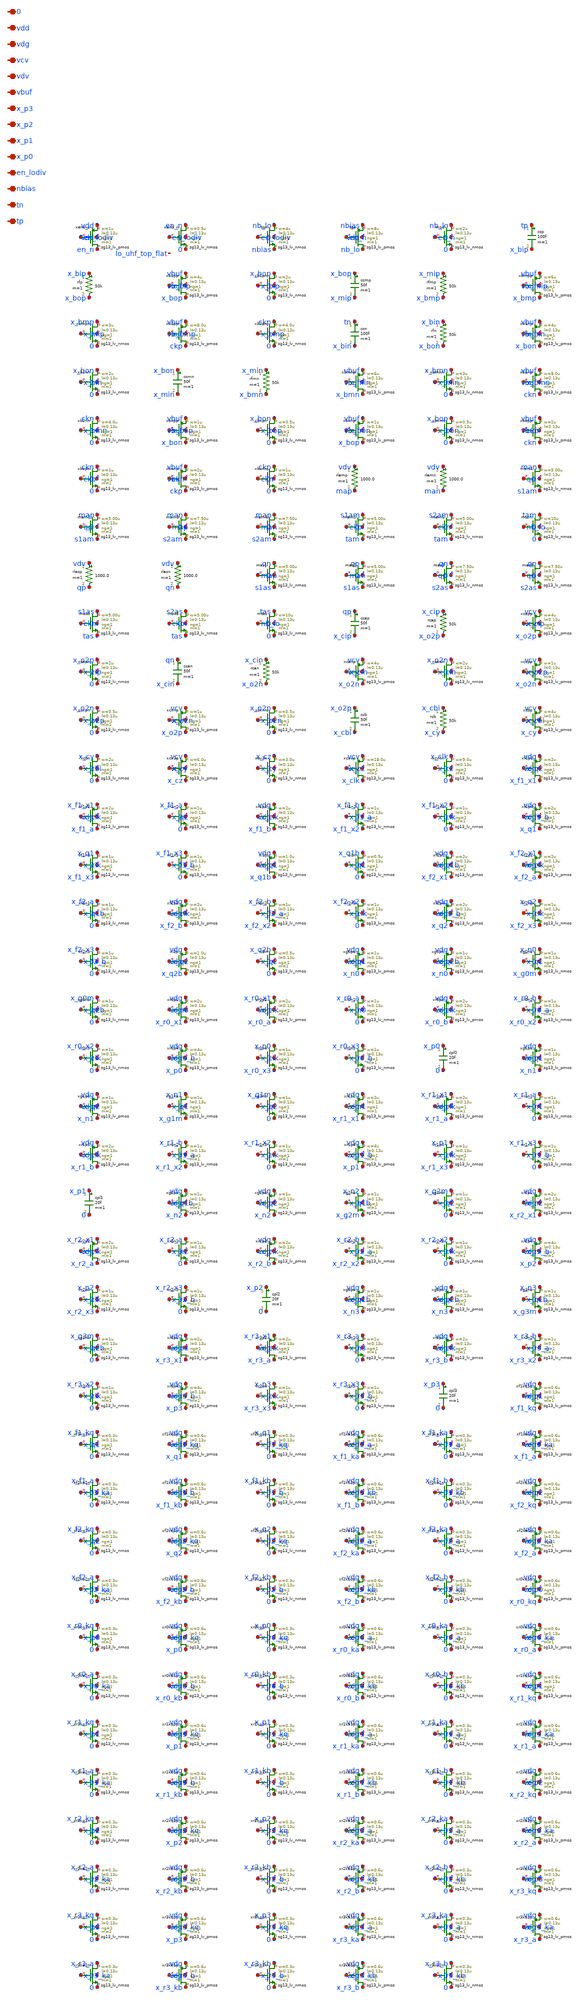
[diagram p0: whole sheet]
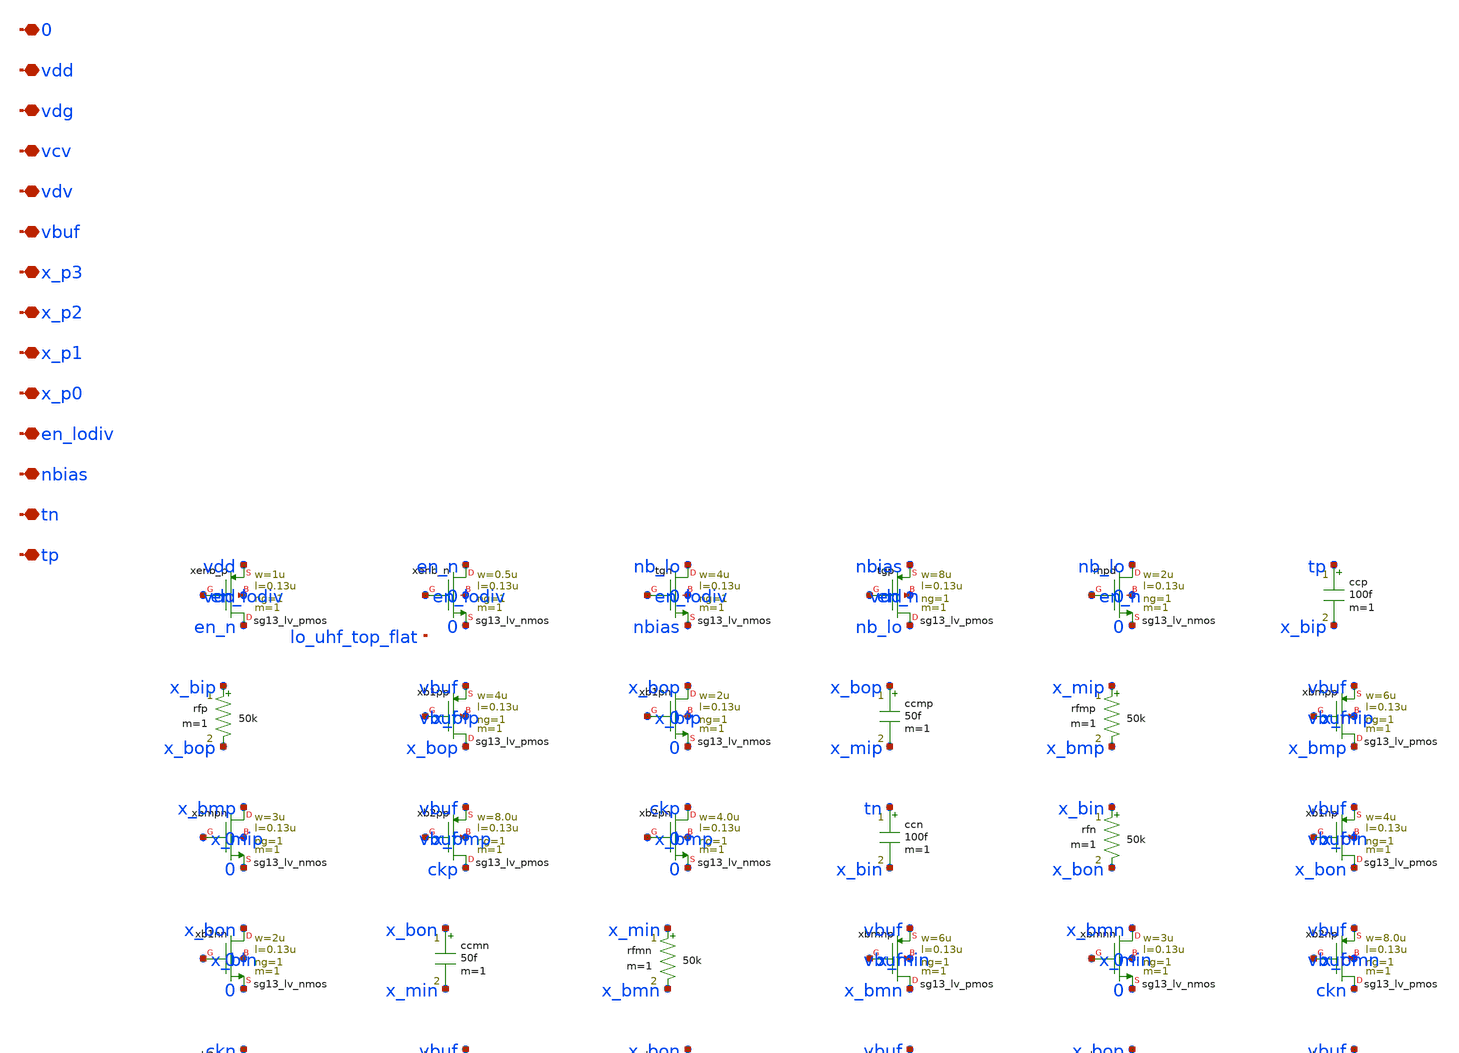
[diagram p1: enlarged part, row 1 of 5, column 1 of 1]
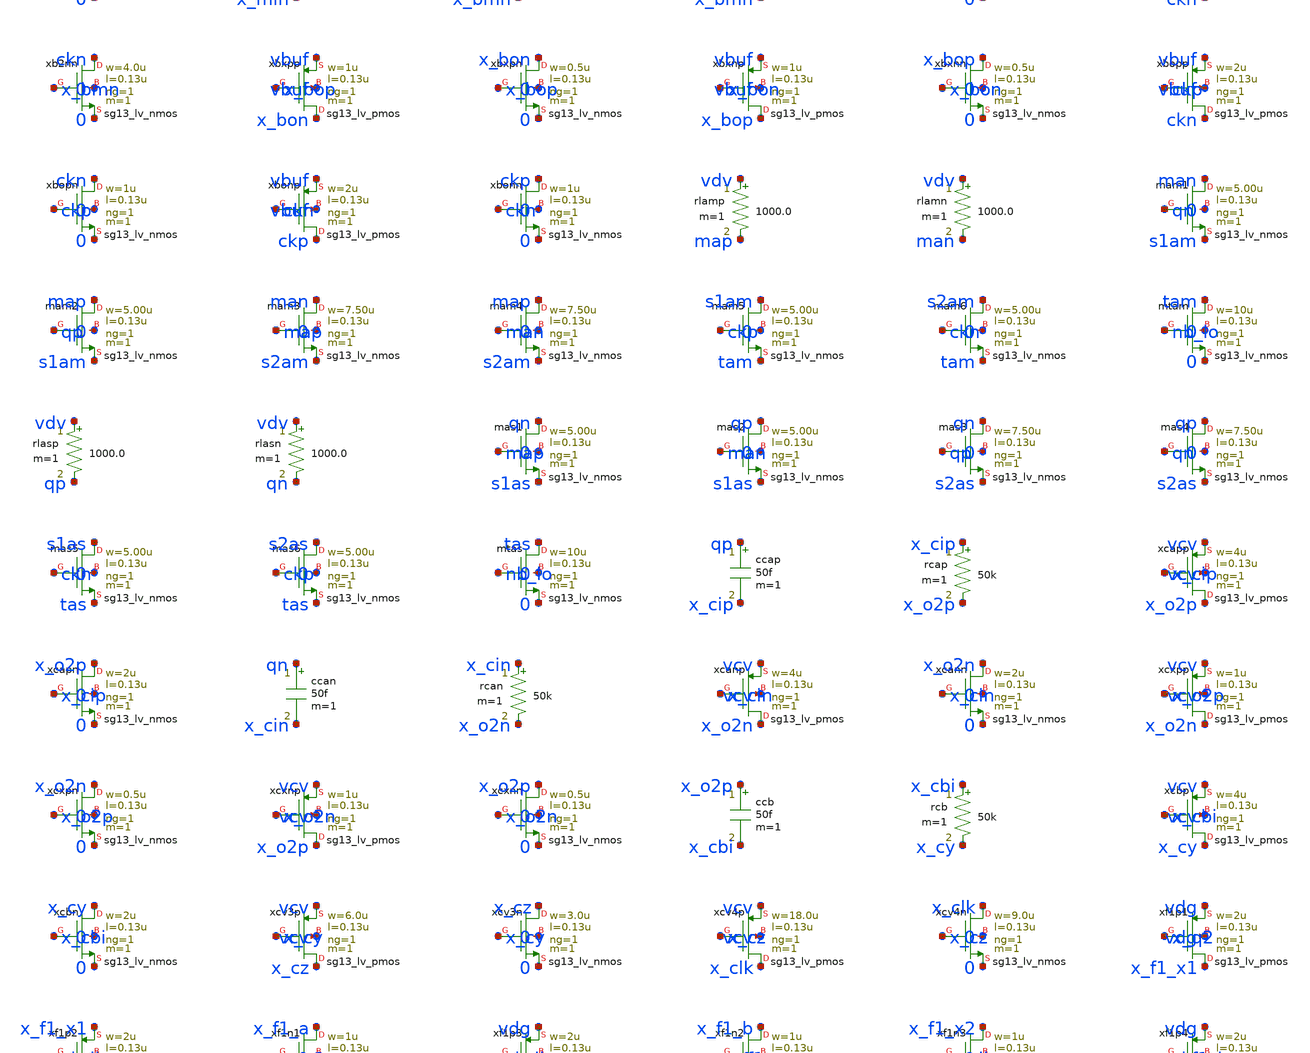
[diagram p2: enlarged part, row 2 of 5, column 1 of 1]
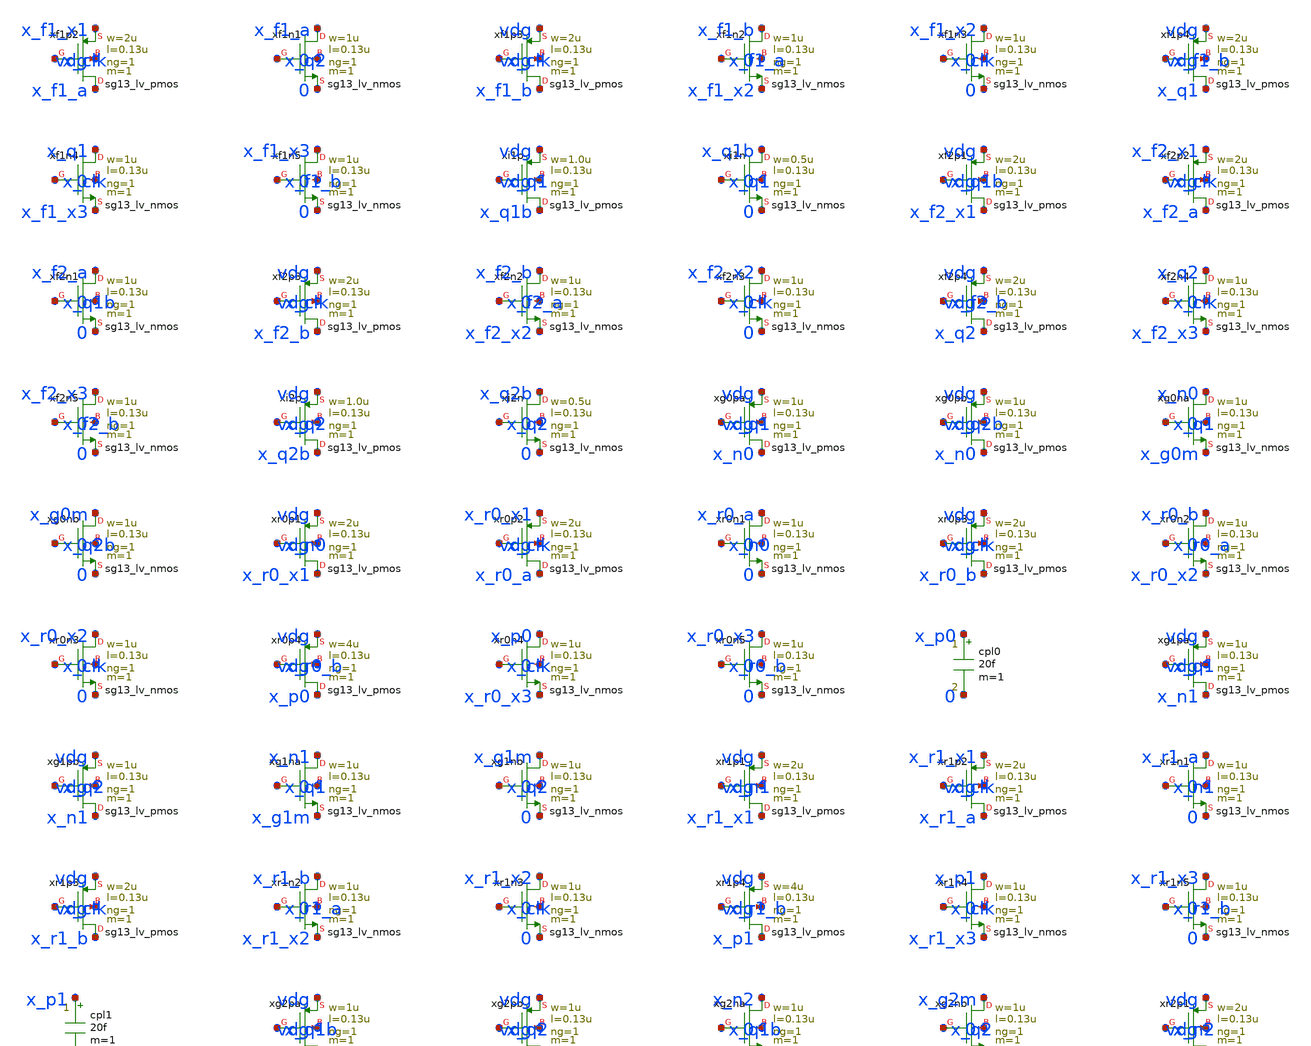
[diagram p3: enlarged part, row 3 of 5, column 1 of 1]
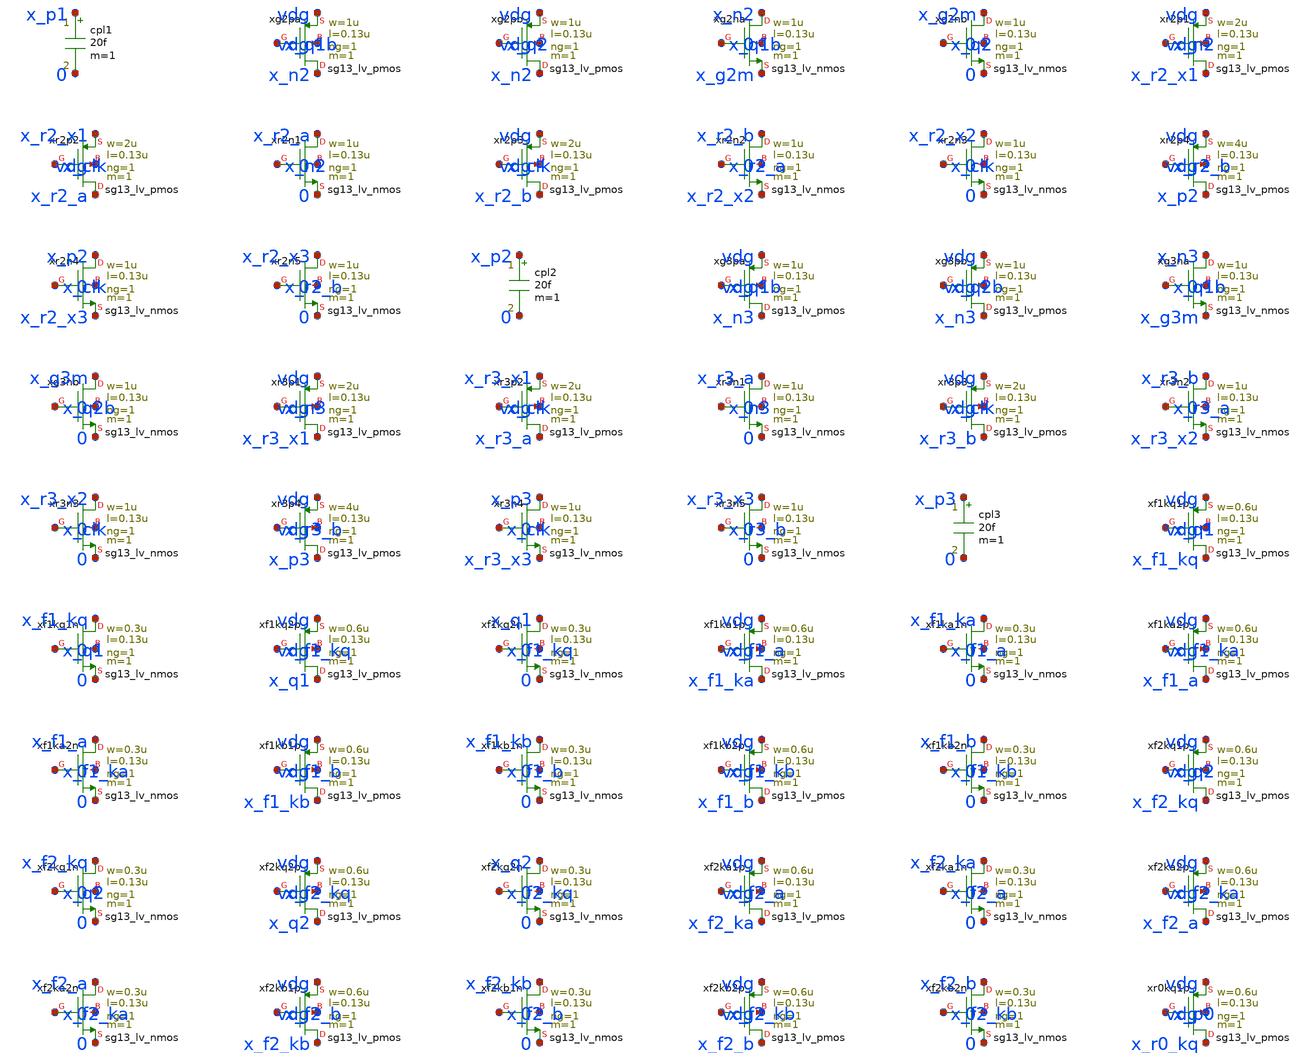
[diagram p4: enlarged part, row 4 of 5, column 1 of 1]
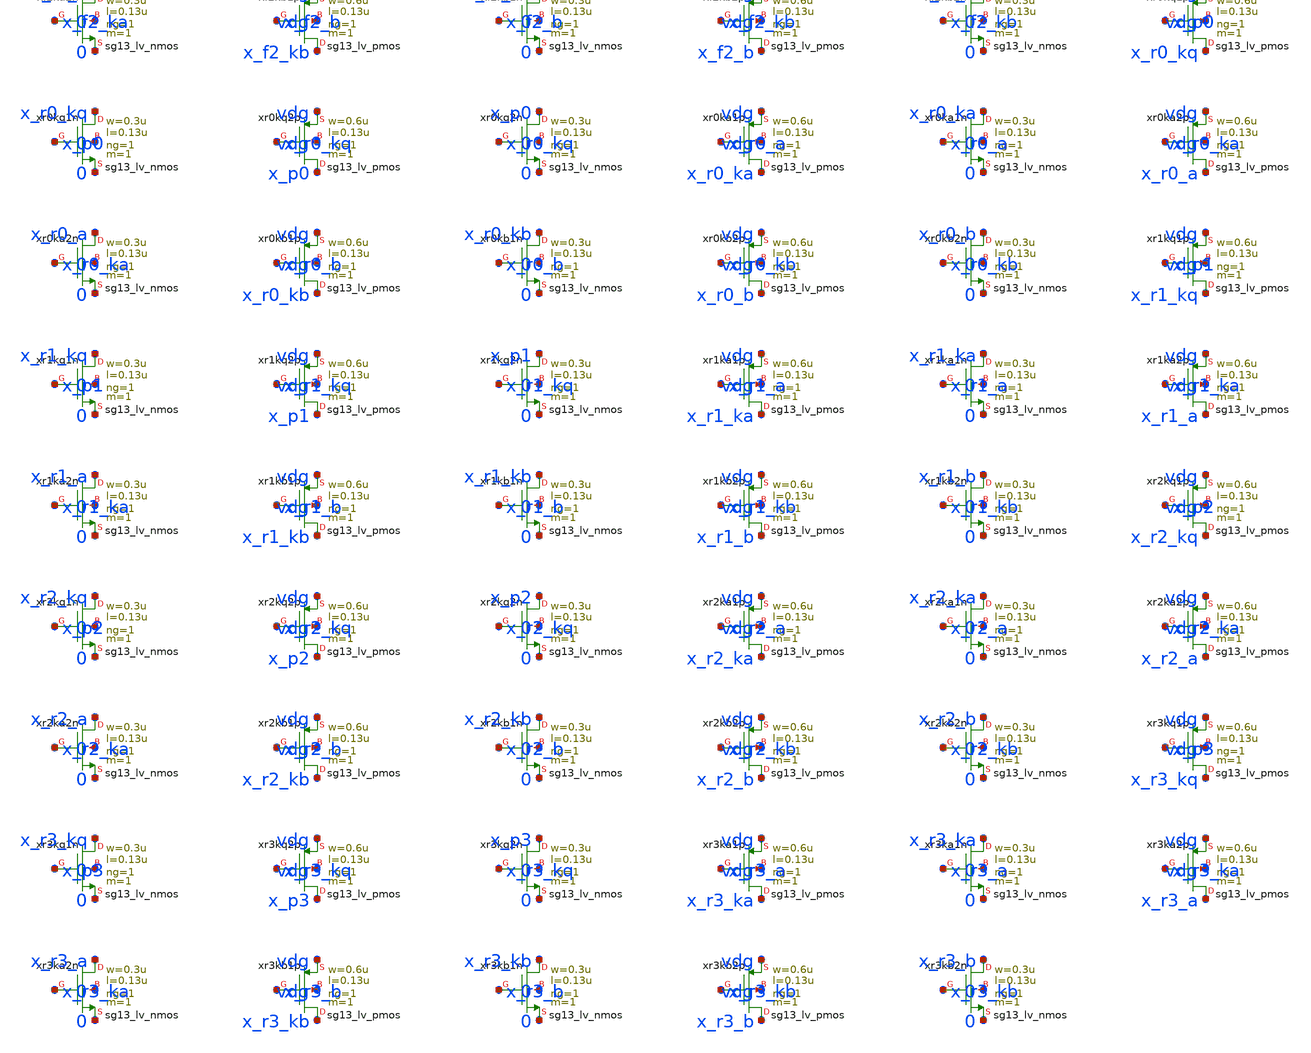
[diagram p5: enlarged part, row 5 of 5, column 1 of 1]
** sch_path: analog/lo/sch/lo_uhf_top.sch
**.subckt lo_uhf_top tp tn nbias en_lodiv x_p0 x_p1 x_p2 x_p3 vbuf vdv vcv vdg vdd 0
*.iopin tp
*.iopin tn
*.iopin nbias
*.iopin en_lodiv
*.iopin x_p0
*.iopin x_p1
*.iopin x_p2
*.iopin x_p3
*.iopin vbuf
*.iopin vdv
*.iopin vcv
*.iopin vdg
*.iopin vdd
*.iopin 0
Xxenb_p en_n en_lodiv vdd vdd sg13_lv_pmos w=1u l=0.13u ng=1 m=1 mm_ok=1
Xxenb_n en_n en_lodiv 0 0 sg13_lv_nmos w=0.5u l=0.13u ng=1 m=1 mm_ok=1
Xtgn nb_lo en_lodiv nbias 0 sg13_lv_nmos w=4u l=0.13u ng=1 m=1 mm_ok=1
Xtgp nb_lo en_n nbias vdd sg13_lv_pmos w=8u l=0.13u ng=1 m=1 mm_ok=1
Xmpd nb_lo en_n 0 0 sg13_lv_nmos w=2u l=0.13u ng=1 m=1 mm_ok=1
ccp tp x_bip 100f m=1
rfp x_bip x_bop 50k m=1
Xxb1pp x_bop x_bip vbuf vbuf sg13_lv_pmos w=4u l=0.13u ng=1 m=1 mm_ok=1
Xxb1pn x_bop x_bip 0 0 sg13_lv_nmos w=2u l=0.13u ng=1 m=1 mm_ok=1
ccmp x_bop x_mip 50f m=1
rfmp x_mip x_bmp 50k m=1
Xxbmpp x_bmp x_mip vbuf vbuf sg13_lv_pmos w=6u l=0.13u ng=1 m=1 mm_ok=1
Xxbmpn x_bmp x_mip 0 0 sg13_lv_nmos w=3u l=0.13u ng=1 m=1 mm_ok=1
Xxb2pp ckp x_bmp vbuf vbuf sg13_lv_pmos w=8.0u l=0.13u ng=1 m=1 mm_ok=1
Xxb2pn ckp x_bmp 0 0 sg13_lv_nmos w=4.0u l=0.13u ng=1 m=1 mm_ok=1
ccn tn x_bin 100f m=1
rfn x_bin x_bon 50k m=1
Xxb1np x_bon x_bin vbuf vbuf sg13_lv_pmos w=4u l=0.13u ng=1 m=1 mm_ok=1
Xxb1nn x_bon x_bin 0 0 sg13_lv_nmos w=2u l=0.13u ng=1 m=1 mm_ok=1
ccmn x_bon x_min 50f m=1
rfmn x_min x_bmn 50k m=1
Xxbmnp x_bmn x_min vbuf vbuf sg13_lv_pmos w=6u l=0.13u ng=1 m=1 mm_ok=1
Xxbmnn x_bmn x_min 0 0 sg13_lv_nmos w=3u l=0.13u ng=1 m=1 mm_ok=1
Xxb2np ckn x_bmn vbuf vbuf sg13_lv_pmos w=8.0u l=0.13u ng=1 m=1 mm_ok=1
Xxb2nn ckn x_bmn 0 0 sg13_lv_nmos w=4.0u l=0.13u ng=1 m=1 mm_ok=1
Xxbxpp x_bon x_bop vbuf vbuf sg13_lv_pmos w=1u l=0.13u ng=1 m=1 mm_ok=1
Xxbxpn x_bon x_bop 0 0 sg13_lv_nmos w=0.5u l=0.13u ng=1 m=1 mm_ok=1
Xxbxnp x_bop x_bon vbuf vbuf sg13_lv_pmos w=1u l=0.13u ng=1 m=1 mm_ok=1
Xxbxnn x_bop x_bon 0 0 sg13_lv_nmos w=0.5u l=0.13u ng=1 m=1 mm_ok=1
Xxbopp ckn ckp vbuf vbuf sg13_lv_pmos w=2u l=0.13u ng=1 m=1 mm_ok=1
Xxbopn ckn ckp 0 0 sg13_lv_nmos w=1u l=0.13u ng=1 m=1 mm_ok=1
Xxbonp ckp ckn vbuf vbuf sg13_lv_pmos w=2u l=0.13u ng=1 m=1 mm_ok=1
Xxbonn ckp ckn 0 0 sg13_lv_nmos w=1u l=0.13u ng=1 m=1 mm_ok=1
rlamp vdv map 1000.0 m=1
rlamn vdv man 1000.0 m=1
Xmam1 man qn s1am 0 sg13_lv_nmos w=5.00u l=0.13u ng=1 m=1 mm_ok=1
Xmam2 map qp s1am 0 sg13_lv_nmos w=5.00u l=0.13u ng=1 m=1 mm_ok=1
Xmam3 man map s2am 0 sg13_lv_nmos w=7.50u l=0.13u ng=1 m=1 mm_ok=1
Xmam4 map man s2am 0 sg13_lv_nmos w=7.50u l=0.13u ng=1 m=1 mm_ok=1
Xmam5 s1am ckp tam 0 sg13_lv_nmos w=5.00u l=0.13u ng=1 m=1 mm_ok=1
Xmam6 s2am ckn tam 0 sg13_lv_nmos w=5.00u l=0.13u ng=1 m=1 mm_ok=1
Xmtam tam nb_lo 0 0 sg13_lv_nmos w=10u l=0.13u ng=1 m=1 mm_ok=1
rlasp vdv qp 1000.0 m=1
rlasn vdv qn 1000.0 m=1
Xmas1 qn map s1as 0 sg13_lv_nmos w=5.00u l=0.13u ng=1 m=1 mm_ok=1
Xmas2 qp man s1as 0 sg13_lv_nmos w=5.00u l=0.13u ng=1 m=1 mm_ok=1
Xmas3 qn qp s2as 0 sg13_lv_nmos w=7.50u l=0.13u ng=1 m=1 mm_ok=1
Xmas4 qp qn s2as 0 sg13_lv_nmos w=7.50u l=0.13u ng=1 m=1 mm_ok=1
Xmas5 s1as ckn tas 0 sg13_lv_nmos w=5.00u l=0.13u ng=1 m=1 mm_ok=1
Xmas6 s2as ckp tas 0 sg13_lv_nmos w=5.00u l=0.13u ng=1 m=1 mm_ok=1
Xmtas tas nb_lo 0 0 sg13_lv_nmos w=10u l=0.13u ng=1 m=1 mm_ok=1
ccap qp x_cip 50f m=1
rcap x_cip x_o2p 50k m=1
Xxcapp x_o2p x_cip vcv vcv sg13_lv_pmos w=4u l=0.13u ng=1 m=1 mm_ok=1
Xxcapn x_o2p x_cip 0 0 sg13_lv_nmos w=2u l=0.13u ng=1 m=1 mm_ok=1
ccan qn x_cin 50f m=1
rcan x_cin x_o2n 50k m=1
Xxcanp x_o2n x_cin vcv vcv sg13_lv_pmos w=4u l=0.13u ng=1 m=1 mm_ok=1
Xxcann x_o2n x_cin 0 0 sg13_lv_nmos w=2u l=0.13u ng=1 m=1 mm_ok=1
Xxcxpp x_o2n x_o2p vcv vcv sg13_lv_pmos w=1u l=0.13u ng=1 m=1 mm_ok=1
Xxcxpn x_o2n x_o2p 0 0 sg13_lv_nmos w=0.5u l=0.13u ng=1 m=1 mm_ok=1
Xxcxnp x_o2p x_o2n vcv vcv sg13_lv_pmos w=1u l=0.13u ng=1 m=1 mm_ok=1
Xxcxnn x_o2p x_o2n 0 0 sg13_lv_nmos w=0.5u l=0.13u ng=1 m=1 mm_ok=1
ccb x_o2p x_cbi 50f m=1
rcb x_cbi x_cy 50k m=1
Xxcbp x_cy x_cbi vcv vcv sg13_lv_pmos w=4u l=0.13u ng=1 m=1 mm_ok=1
Xxcbn x_cy x_cbi 0 0 sg13_lv_nmos w=2u l=0.13u ng=1 m=1 mm_ok=1
Xxcv3p x_cz x_cy vcv vcv sg13_lv_pmos w=6.0u l=0.13u ng=1 m=1 mm_ok=1
Xxcv3n x_cz x_cy 0 0 sg13_lv_nmos w=3.0u l=0.13u ng=1 m=1 mm_ok=1
Xxcv4p x_clk x_cz vcv vcv sg13_lv_pmos w=18.0u l=0.13u ng=1 m=1 mm_ok=1
Xxcv4n x_clk x_cz 0 0 sg13_lv_nmos w=9.0u l=0.13u ng=1 m=1 mm_ok=1
Xxf1p1 x_f1_x1 x_q2 vdg vdg sg13_lv_pmos w=2u l=0.13u ng=1 m=1 mm_ok=1
Xxf1p2 x_f1_a x_clk x_f1_x1 vdg sg13_lv_pmos w=2u l=0.13u ng=1 m=1 mm_ok=1
Xxf1n1 x_f1_a x_q2 0 0 sg13_lv_nmos w=1u l=0.13u ng=1 m=1 mm_ok=1
Xxf1p3 x_f1_b x_clk vdg vdg sg13_lv_pmos w=2u l=0.13u ng=1 m=1 mm_ok=1
Xxf1n2 x_f1_b x_f1_a x_f1_x2 0 sg13_lv_nmos w=1u l=0.13u ng=1 m=1 mm_ok=1
Xxf1n3 x_f1_x2 x_clk 0 0 sg13_lv_nmos w=1u l=0.13u ng=1 m=1 mm_ok=1
Xxf1p4 x_q1 x_f1_b vdg vdg sg13_lv_pmos w=2u l=0.13u ng=1 m=1 mm_ok=1
Xxf1n4 x_q1 x_clk x_f1_x3 0 sg13_lv_nmos w=1u l=0.13u ng=1 m=1 mm_ok=1
Xxf1n5 x_f1_x3 x_f1_b 0 0 sg13_lv_nmos w=1u l=0.13u ng=1 m=1 mm_ok=1
Xxi1p x_q1b x_q1 vdg vdg sg13_lv_pmos w=1.0u l=0.13u ng=1 m=1 mm_ok=1
Xxi1n x_q1b x_q1 0 0 sg13_lv_nmos w=0.5u l=0.13u ng=1 m=1 mm_ok=1
Xxf2p1 x_f2_x1 x_q1b vdg vdg sg13_lv_pmos w=2u l=0.13u ng=1 m=1 mm_ok=1
Xxf2p2 x_f2_a x_clk x_f2_x1 vdg sg13_lv_pmos w=2u l=0.13u ng=1 m=1 mm_ok=1
Xxf2n1 x_f2_a x_q1b 0 0 sg13_lv_nmos w=1u l=0.13u ng=1 m=1 mm_ok=1
Xxf2p3 x_f2_b x_clk vdg vdg sg13_lv_pmos w=2u l=0.13u ng=1 m=1 mm_ok=1
Xxf2n2 x_f2_b x_f2_a x_f2_x2 0 sg13_lv_nmos w=1u l=0.13u ng=1 m=1 mm_ok=1
Xxf2n3 x_f2_x2 x_clk 0 0 sg13_lv_nmos w=1u l=0.13u ng=1 m=1 mm_ok=1
Xxf2p4 x_q2 x_f2_b vdg vdg sg13_lv_pmos w=2u l=0.13u ng=1 m=1 mm_ok=1
Xxf2n4 x_q2 x_clk x_f2_x3 0 sg13_lv_nmos w=1u l=0.13u ng=1 m=1 mm_ok=1
Xxf2n5 x_f2_x3 x_f2_b 0 0 sg13_lv_nmos w=1u l=0.13u ng=1 m=1 mm_ok=1
Xxi2p x_q2b x_q2 vdg vdg sg13_lv_pmos w=1.0u l=0.13u ng=1 m=1 mm_ok=1
Xxi2n x_q2b x_q2 0 0 sg13_lv_nmos w=0.5u l=0.13u ng=1 m=1 mm_ok=1
Xxg0pa x_n0 x_q1 vdg vdg sg13_lv_pmos w=1u l=0.13u ng=1 m=1 mm_ok=1
Xxg0pb x_n0 x_q2b vdg vdg sg13_lv_pmos w=1u l=0.13u ng=1 m=1 mm_ok=1
Xxg0na x_n0 x_q1 x_g0m 0 sg13_lv_nmos w=1u l=0.13u ng=1 m=1 mm_ok=1
Xxg0nb x_g0m x_q2b 0 0 sg13_lv_nmos w=1u l=0.13u ng=1 m=1 mm_ok=1
Xxr0p1 x_r0_x1 x_n0 vdg vdg sg13_lv_pmos w=2u l=0.13u ng=1 m=1 mm_ok=1
Xxr0p2 x_r0_a x_clk x_r0_x1 vdg sg13_lv_pmos w=2u l=0.13u ng=1 m=1 mm_ok=1
Xxr0n1 x_r0_a x_n0 0 0 sg13_lv_nmos w=1u l=0.13u ng=1 m=1 mm_ok=1
Xxr0p3 x_r0_b x_clk vdg vdg sg13_lv_pmos w=2u l=0.13u ng=1 m=1 mm_ok=1
Xxr0n2 x_r0_b x_r0_a x_r0_x2 0 sg13_lv_nmos w=1u l=0.13u ng=1 m=1 mm_ok=1
Xxr0n3 x_r0_x2 x_clk 0 0 sg13_lv_nmos w=1u l=0.13u ng=1 m=1 mm_ok=1
Xxr0p4 x_p0 x_r0_b vdg vdg sg13_lv_pmos w=4u l=0.13u ng=1 m=1 mm_ok=1
Xxr0n4 x_p0 x_clk x_r0_x3 0 sg13_lv_nmos w=1u l=0.13u ng=1 m=1 mm_ok=1
Xxr0n5 x_r0_x3 x_r0_b 0 0 sg13_lv_nmos w=1u l=0.13u ng=1 m=1 mm_ok=1
cpl0 x_p0 0 20f m=1
Xxg1pa x_n1 x_q1 vdg vdg sg13_lv_pmos w=1u l=0.13u ng=1 m=1 mm_ok=1
Xxg1pb x_n1 x_q2 vdg vdg sg13_lv_pmos w=1u l=0.13u ng=1 m=1 mm_ok=1
Xxg1na x_n1 x_q1 x_g1m 0 sg13_lv_nmos w=1u l=0.13u ng=1 m=1 mm_ok=1
Xxg1nb x_g1m x_q2 0 0 sg13_lv_nmos w=1u l=0.13u ng=1 m=1 mm_ok=1
Xxr1p1 x_r1_x1 x_n1 vdg vdg sg13_lv_pmos w=2u l=0.13u ng=1 m=1 mm_ok=1
Xxr1p2 x_r1_a x_clk x_r1_x1 vdg sg13_lv_pmos w=2u l=0.13u ng=1 m=1 mm_ok=1
Xxr1n1 x_r1_a x_n1 0 0 sg13_lv_nmos w=1u l=0.13u ng=1 m=1 mm_ok=1
Xxr1p3 x_r1_b x_clk vdg vdg sg13_lv_pmos w=2u l=0.13u ng=1 m=1 mm_ok=1
Xxr1n2 x_r1_b x_r1_a x_r1_x2 0 sg13_lv_nmos w=1u l=0.13u ng=1 m=1 mm_ok=1
Xxr1n3 x_r1_x2 x_clk 0 0 sg13_lv_nmos w=1u l=0.13u ng=1 m=1 mm_ok=1
Xxr1p4 x_p1 x_r1_b vdg vdg sg13_lv_pmos w=4u l=0.13u ng=1 m=1 mm_ok=1
Xxr1n4 x_p1 x_clk x_r1_x3 0 sg13_lv_nmos w=1u l=0.13u ng=1 m=1 mm_ok=1
Xxr1n5 x_r1_x3 x_r1_b 0 0 sg13_lv_nmos w=1u l=0.13u ng=1 m=1 mm_ok=1
cpl1 x_p1 0 20f m=1
Xxg2pa x_n2 x_q1b vdg vdg sg13_lv_pmos w=1u l=0.13u ng=1 m=1 mm_ok=1
Xxg2pb x_n2 x_q2 vdg vdg sg13_lv_pmos w=1u l=0.13u ng=1 m=1 mm_ok=1
Xxg2na x_n2 x_q1b x_g2m 0 sg13_lv_nmos w=1u l=0.13u ng=1 m=1 mm_ok=1
Xxg2nb x_g2m x_q2 0 0 sg13_lv_nmos w=1u l=0.13u ng=1 m=1 mm_ok=1
Xxr2p1 x_r2_x1 x_n2 vdg vdg sg13_lv_pmos w=2u l=0.13u ng=1 m=1 mm_ok=1
Xxr2p2 x_r2_a x_clk x_r2_x1 vdg sg13_lv_pmos w=2u l=0.13u ng=1 m=1 mm_ok=1
Xxr2n1 x_r2_a x_n2 0 0 sg13_lv_nmos w=1u l=0.13u ng=1 m=1 mm_ok=1
Xxr2p3 x_r2_b x_clk vdg vdg sg13_lv_pmos w=2u l=0.13u ng=1 m=1 mm_ok=1
Xxr2n2 x_r2_b x_r2_a x_r2_x2 0 sg13_lv_nmos w=1u l=0.13u ng=1 m=1 mm_ok=1
Xxr2n3 x_r2_x2 x_clk 0 0 sg13_lv_nmos w=1u l=0.13u ng=1 m=1 mm_ok=1
Xxr2p4 x_p2 x_r2_b vdg vdg sg13_lv_pmos w=4u l=0.13u ng=1 m=1 mm_ok=1
Xxr2n4 x_p2 x_clk x_r2_x3 0 sg13_lv_nmos w=1u l=0.13u ng=1 m=1 mm_ok=1
Xxr2n5 x_r2_x3 x_r2_b 0 0 sg13_lv_nmos w=1u l=0.13u ng=1 m=1 mm_ok=1
cpl2 x_p2 0 20f m=1
Xxg3pa x_n3 x_q1b vdg vdg sg13_lv_pmos w=1u l=0.13u ng=1 m=1 mm_ok=1
Xxg3pb x_n3 x_q2b vdg vdg sg13_lv_pmos w=1u l=0.13u ng=1 m=1 mm_ok=1
Xxg3na x_n3 x_q1b x_g3m 0 sg13_lv_nmos w=1u l=0.13u ng=1 m=1 mm_ok=1
Xxg3nb x_g3m x_q2b 0 0 sg13_lv_nmos w=1u l=0.13u ng=1 m=1 mm_ok=1
Xxr3p1 x_r3_x1 x_n3 vdg vdg sg13_lv_pmos w=2u l=0.13u ng=1 m=1 mm_ok=1
Xxr3p2 x_r3_a x_clk x_r3_x1 vdg sg13_lv_pmos w=2u l=0.13u ng=1 m=1 mm_ok=1
Xxr3n1 x_r3_a x_n3 0 0 sg13_lv_nmos w=1u l=0.13u ng=1 m=1 mm_ok=1
Xxr3p3 x_r3_b x_clk vdg vdg sg13_lv_pmos w=2u l=0.13u ng=1 m=1 mm_ok=1
Xxr3n2 x_r3_b x_r3_a x_r3_x2 0 sg13_lv_nmos w=1u l=0.13u ng=1 m=1 mm_ok=1
Xxr3n3 x_r3_x2 x_clk 0 0 sg13_lv_nmos w=1u l=0.13u ng=1 m=1 mm_ok=1
Xxr3p4 x_p3 x_r3_b vdg vdg sg13_lv_pmos w=4u l=0.13u ng=1 m=1 mm_ok=1
Xxr3n4 x_p3 x_clk x_r3_x3 0 sg13_lv_nmos w=1u l=0.13u ng=1 m=1 mm_ok=1
Xxr3n5 x_r3_x3 x_r3_b 0 0 sg13_lv_nmos w=1u l=0.13u ng=1 m=1 mm_ok=1
cpl3 x_p3 0 20f m=1
Xxf1kq1p x_f1_kq x_q1 vdg vdg sg13_lv_pmos w=0.6u l=0.13u ng=1 m=1 mm_ok=1
Xxf1kq1n x_f1_kq x_q1 0 0 sg13_lv_nmos w=0.3u l=0.13u ng=1 m=1 mm_ok=1
Xxf1kq2p x_q1 x_f1_kq vdg vdg sg13_lv_pmos w=0.6u l=0.13u ng=1 m=1 mm_ok=1
Xxf1kq2n x_q1 x_f1_kq 0 0 sg13_lv_nmos w=0.3u l=0.13u ng=1 m=1 mm_ok=1
Xxf1ka1p x_f1_ka x_f1_a vdg vdg sg13_lv_pmos w=0.6u l=0.13u ng=1 m=1 mm_ok=1
Xxf1ka1n x_f1_ka x_f1_a 0 0 sg13_lv_nmos w=0.3u l=0.13u ng=1 m=1 mm_ok=1
Xxf1ka2p x_f1_a x_f1_ka vdg vdg sg13_lv_pmos w=0.6u l=0.13u ng=1 m=1 mm_ok=1
Xxf1ka2n x_f1_a x_f1_ka 0 0 sg13_lv_nmos w=0.3u l=0.13u ng=1 m=1 mm_ok=1
Xxf1kb1p x_f1_kb x_f1_b vdg vdg sg13_lv_pmos w=0.6u l=0.13u ng=1 m=1 mm_ok=1
Xxf1kb1n x_f1_kb x_f1_b 0 0 sg13_lv_nmos w=0.3u l=0.13u ng=1 m=1 mm_ok=1
Xxf1kb2p x_f1_b x_f1_kb vdg vdg sg13_lv_pmos w=0.6u l=0.13u ng=1 m=1 mm_ok=1
Xxf1kb2n x_f1_b x_f1_kb 0 0 sg13_lv_nmos w=0.3u l=0.13u ng=1 m=1 mm_ok=1
Xxf2kq1p x_f2_kq x_q2 vdg vdg sg13_lv_pmos w=0.6u l=0.13u ng=1 m=1 mm_ok=1
Xxf2kq1n x_f2_kq x_q2 0 0 sg13_lv_nmos w=0.3u l=0.13u ng=1 m=1 mm_ok=1
Xxf2kq2p x_q2 x_f2_kq vdg vdg sg13_lv_pmos w=0.6u l=0.13u ng=1 m=1 mm_ok=1
Xxf2kq2n x_q2 x_f2_kq 0 0 sg13_lv_nmos w=0.3u l=0.13u ng=1 m=1 mm_ok=1
Xxf2ka1p x_f2_ka x_f2_a vdg vdg sg13_lv_pmos w=0.6u l=0.13u ng=1 m=1 mm_ok=1
Xxf2ka1n x_f2_ka x_f2_a 0 0 sg13_lv_nmos w=0.3u l=0.13u ng=1 m=1 mm_ok=1
Xxf2ka2p x_f2_a x_f2_ka vdg vdg sg13_lv_pmos w=0.6u l=0.13u ng=1 m=1 mm_ok=1
Xxf2ka2n x_f2_a x_f2_ka 0 0 sg13_lv_nmos w=0.3u l=0.13u ng=1 m=1 mm_ok=1
Xxf2kb1p x_f2_kb x_f2_b vdg vdg sg13_lv_pmos w=0.6u l=0.13u ng=1 m=1 mm_ok=1
Xxf2kb1n x_f2_kb x_f2_b 0 0 sg13_lv_nmos w=0.3u l=0.13u ng=1 m=1 mm_ok=1
Xxf2kb2p x_f2_b x_f2_kb vdg vdg sg13_lv_pmos w=0.6u l=0.13u ng=1 m=1 mm_ok=1
Xxf2kb2n x_f2_b x_f2_kb 0 0 sg13_lv_nmos w=0.3u l=0.13u ng=1 m=1 mm_ok=1
Xxr0kq1p x_r0_kq x_p0 vdg vdg sg13_lv_pmos w=0.6u l=0.13u ng=1 m=1 mm_ok=1
Xxr0kq1n x_r0_kq x_p0 0 0 sg13_lv_nmos w=0.3u l=0.13u ng=1 m=1 mm_ok=1
Xxr0kq2p x_p0 x_r0_kq vdg vdg sg13_lv_pmos w=0.6u l=0.13u ng=1 m=1 mm_ok=1
Xxr0kq2n x_p0 x_r0_kq 0 0 sg13_lv_nmos w=0.3u l=0.13u ng=1 m=1 mm_ok=1
Xxr0ka1p x_r0_ka x_r0_a vdg vdg sg13_lv_pmos w=0.6u l=0.13u ng=1 m=1 mm_ok=1
Xxr0ka1n x_r0_ka x_r0_a 0 0 sg13_lv_nmos w=0.3u l=0.13u ng=1 m=1 mm_ok=1
Xxr0ka2p x_r0_a x_r0_ka vdg vdg sg13_lv_pmos w=0.6u l=0.13u ng=1 m=1 mm_ok=1
Xxr0ka2n x_r0_a x_r0_ka 0 0 sg13_lv_nmos w=0.3u l=0.13u ng=1 m=1 mm_ok=1
Xxr0kb1p x_r0_kb x_r0_b vdg vdg sg13_lv_pmos w=0.6u l=0.13u ng=1 m=1 mm_ok=1
Xxr0kb1n x_r0_kb x_r0_b 0 0 sg13_lv_nmos w=0.3u l=0.13u ng=1 m=1 mm_ok=1
Xxr0kb2p x_r0_b x_r0_kb vdg vdg sg13_lv_pmos w=0.6u l=0.13u ng=1 m=1 mm_ok=1
Xxr0kb2n x_r0_b x_r0_kb 0 0 sg13_lv_nmos w=0.3u l=0.13u ng=1 m=1 mm_ok=1
Xxr1kq1p x_r1_kq x_p1 vdg vdg sg13_lv_pmos w=0.6u l=0.13u ng=1 m=1 mm_ok=1
Xxr1kq1n x_r1_kq x_p1 0 0 sg13_lv_nmos w=0.3u l=0.13u ng=1 m=1 mm_ok=1
Xxr1kq2p x_p1 x_r1_kq vdg vdg sg13_lv_pmos w=0.6u l=0.13u ng=1 m=1 mm_ok=1
Xxr1kq2n x_p1 x_r1_kq 0 0 sg13_lv_nmos w=0.3u l=0.13u ng=1 m=1 mm_ok=1
Xxr1ka1p x_r1_ka x_r1_a vdg vdg sg13_lv_pmos w=0.6u l=0.13u ng=1 m=1 mm_ok=1
Xxr1ka1n x_r1_ka x_r1_a 0 0 sg13_lv_nmos w=0.3u l=0.13u ng=1 m=1 mm_ok=1
Xxr1ka2p x_r1_a x_r1_ka vdg vdg sg13_lv_pmos w=0.6u l=0.13u ng=1 m=1 mm_ok=1
Xxr1ka2n x_r1_a x_r1_ka 0 0 sg13_lv_nmos w=0.3u l=0.13u ng=1 m=1 mm_ok=1
Xxr1kb1p x_r1_kb x_r1_b vdg vdg sg13_lv_pmos w=0.6u l=0.13u ng=1 m=1 mm_ok=1
Xxr1kb1n x_r1_kb x_r1_b 0 0 sg13_lv_nmos w=0.3u l=0.13u ng=1 m=1 mm_ok=1
Xxr1kb2p x_r1_b x_r1_kb vdg vdg sg13_lv_pmos w=0.6u l=0.13u ng=1 m=1 mm_ok=1
Xxr1kb2n x_r1_b x_r1_kb 0 0 sg13_lv_nmos w=0.3u l=0.13u ng=1 m=1 mm_ok=1
Xxr2kq1p x_r2_kq x_p2 vdg vdg sg13_lv_pmos w=0.6u l=0.13u ng=1 m=1 mm_ok=1
Xxr2kq1n x_r2_kq x_p2 0 0 sg13_lv_nmos w=0.3u l=0.13u ng=1 m=1 mm_ok=1
Xxr2kq2p x_p2 x_r2_kq vdg vdg sg13_lv_pmos w=0.6u l=0.13u ng=1 m=1 mm_ok=1
Xxr2kq2n x_p2 x_r2_kq 0 0 sg13_lv_nmos w=0.3u l=0.13u ng=1 m=1 mm_ok=1
Xxr2ka1p x_r2_ka x_r2_a vdg vdg sg13_lv_pmos w=0.6u l=0.13u ng=1 m=1 mm_ok=1
Xxr2ka1n x_r2_ka x_r2_a 0 0 sg13_lv_nmos w=0.3u l=0.13u ng=1 m=1 mm_ok=1
Xxr2ka2p x_r2_a x_r2_ka vdg vdg sg13_lv_pmos w=0.6u l=0.13u ng=1 m=1 mm_ok=1
Xxr2ka2n x_r2_a x_r2_ka 0 0 sg13_lv_nmos w=0.3u l=0.13u ng=1 m=1 mm_ok=1
Xxr2kb1p x_r2_kb x_r2_b vdg vdg sg13_lv_pmos w=0.6u l=0.13u ng=1 m=1 mm_ok=1
Xxr2kb1n x_r2_kb x_r2_b 0 0 sg13_lv_nmos w=0.3u l=0.13u ng=1 m=1 mm_ok=1
Xxr2kb2p x_r2_b x_r2_kb vdg vdg sg13_lv_pmos w=0.6u l=0.13u ng=1 m=1 mm_ok=1
Xxr2kb2n x_r2_b x_r2_kb 0 0 sg13_lv_nmos w=0.3u l=0.13u ng=1 m=1 mm_ok=1
Xxr3kq1p x_r3_kq x_p3 vdg vdg sg13_lv_pmos w=0.6u l=0.13u ng=1 m=1 mm_ok=1
Xxr3kq1n x_r3_kq x_p3 0 0 sg13_lv_nmos w=0.3u l=0.13u ng=1 m=1 mm_ok=1
Xxr3kq2p x_p3 x_r3_kq vdg vdg sg13_lv_pmos w=0.6u l=0.13u ng=1 m=1 mm_ok=1
Xxr3kq2n x_p3 x_r3_kq 0 0 sg13_lv_nmos w=0.3u l=0.13u ng=1 m=1 mm_ok=1
Xxr3ka1p x_r3_ka x_r3_a vdg vdg sg13_lv_pmos w=0.6u l=0.13u ng=1 m=1 mm_ok=1
Xxr3ka1n x_r3_ka x_r3_a 0 0 sg13_lv_nmos w=0.3u l=0.13u ng=1 m=1 mm_ok=1
Xxr3ka2p x_r3_a x_r3_ka vdg vdg sg13_lv_pmos w=0.6u l=0.13u ng=1 m=1 mm_ok=1
Xxr3ka2n x_r3_a x_r3_ka 0 0 sg13_lv_nmos w=0.3u l=0.13u ng=1 m=1 mm_ok=1
Xxr3kb1p x_r3_kb x_r3_b vdg vdg sg13_lv_pmos w=0.6u l=0.13u ng=1 m=1 mm_ok=1
Xxr3kb1n x_r3_kb x_r3_b 0 0 sg13_lv_nmos w=0.3u l=0.13u ng=1 m=1 mm_ok=1
Xxr3kb2p x_r3_b x_r3_kb vdg vdg sg13_lv_pmos w=0.6u l=0.13u ng=1 m=1 mm_ok=1
Xxr3kb2n x_r3_b x_r3_kb 0 0 sg13_lv_nmos w=0.3u l=0.13u ng=1 m=1 mm_ok=1
**.ends
.end
